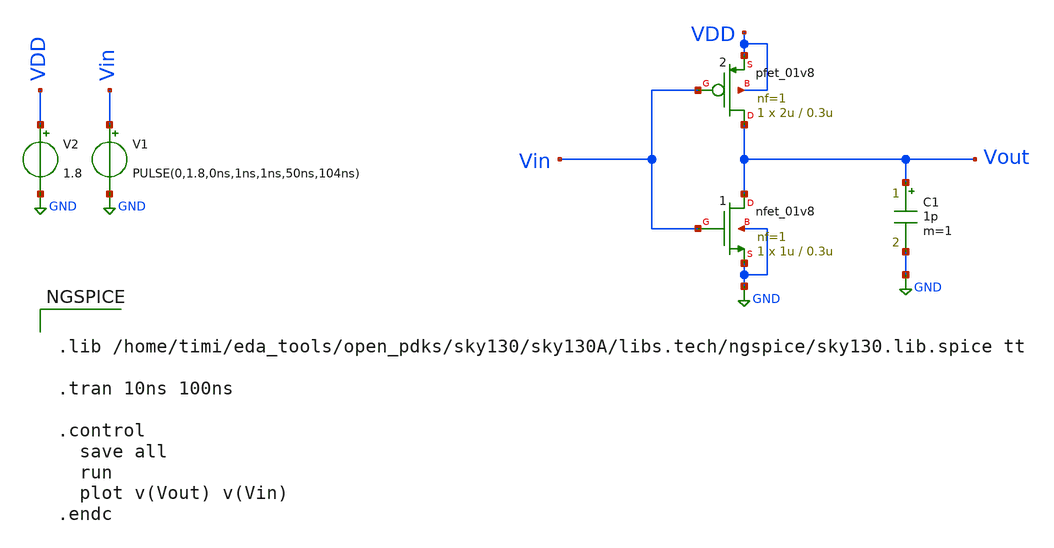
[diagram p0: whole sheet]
** sch_path: schematic-design/inverter.sch
**.subckt inverter
X1 Vout Vin GND GND sky130_fd_pr__nfet_01v8 L=0.3u W=1u nf=1 ad='int((1 + 1)/2) * 1u / 1 * 0.29' as='int((1 + 2)/2) * 1u / 1 * 0.29'
+ pd='2*int((1 + 1)/2) * (1u / 1 + 0.29)' ps='2*int((1 + 2)/2) * (1u / 1 + 0.29)' nrd='0.29 / 1u ' nrs='0.29 / 1u '
+ sa=0 sb=0 sd=0 mult=1 m=1
X2 Vout Vin VDD VDD sky130_fd_pr__pfet_01v8 L=0.3u W=2u nf=1 ad='int((1 + 1)/2) * 2u / 1 * 0.29' as='int((1 + 2)/2) * 2u / 1 * 0.29'
+ pd='2*int((1 + 1)/2) * (2u / 1 + 0.29)' ps='2*int((1 + 2)/2) * (2u / 1 + 0.29)' nrd='0.29 / 2u ' nrs='0.29 / 2u '
+ sa=0 sb=0 sd=0 mult=1 m=1
V1 Vin GND PULSE(0,1.8,0ns,1ns,1ns,50ns,104ns)
V2 VDD GND 1.8
C1 Vout GND 1p m=1
**** begin user architecture code


.lib /home/timi/eda_tools/open_pdks/sky130/sky130A/libs.tech/ngspice/sky130.lib.spice tt

.tran 10ns 100ns

.control
  save all
  run
  plot v(Vout) v(Vin)
.endc


**** end user architecture code
**.ends
.GLOBAL GND
.end
